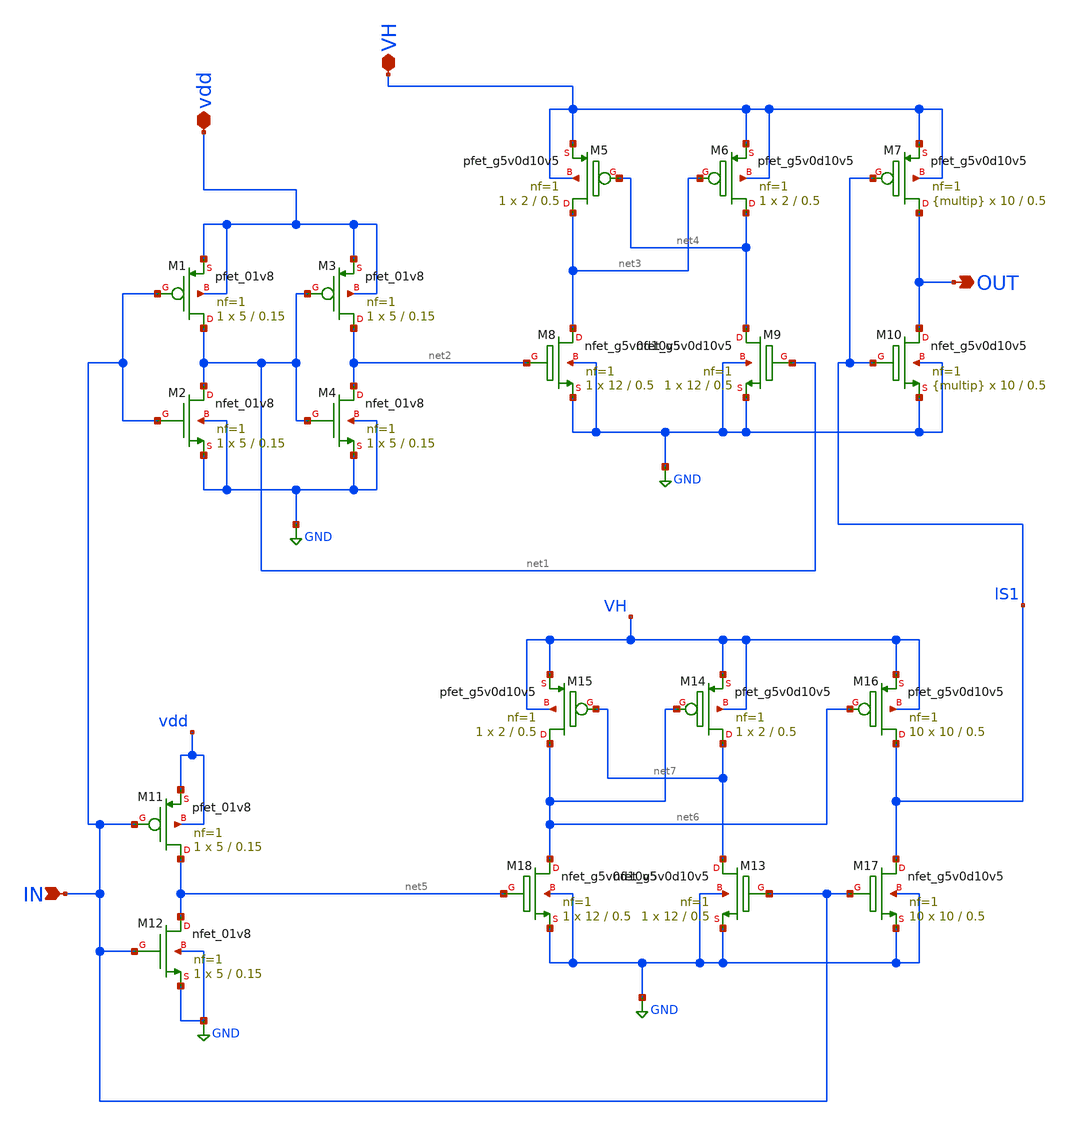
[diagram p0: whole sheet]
** sch_path: xschem/dev_switches/DCDC_10V/LS.sch
**.subckt LS OUT IN VH vdd
*.opin OUT
*.ipin IN
*.iopin VH
*.iopin vdd
XM1 net1 IN vdd vdd sky130_fd_pr__pfet_01v8 L=0.15 W=5 nf=1 ad='int((nf+1)/2) * W/nf * 0.29' as='int((nf+2)/2) * W/nf * 0.29'
+ pd='2*int((nf+1)/2) * (W/nf + 0.29)' ps='2*int((nf+2)/2) * (W/nf + 0.29)' nrd='0.29 / W' nrs='0.29 / W'
+ sa=0 sb=0 sd=0 mult=1 m=1
XM2 net1 IN GND GND sky130_fd_pr__nfet_01v8 L=0.15 W=5 nf=1 ad='int((nf+1)/2) * W/nf * 0.29' as='int((nf+2)/2) * W/nf * 0.29'
+ pd='2*int((nf+1)/2) * (W/nf + 0.29)' ps='2*int((nf+2)/2) * (W/nf + 0.29)' nrd='0.29 / W' nrs='0.29 / W'
+ sa=0 sb=0 sd=0 mult=1 m=1
XM3 net2 net1 vdd vdd sky130_fd_pr__pfet_01v8 L=0.15 W=5 nf=1 ad='int((nf+1)/2) * W/nf * 0.29' as='int((nf+2)/2) * W/nf * 0.29'
+ pd='2*int((nf+1)/2) * (W/nf + 0.29)' ps='2*int((nf+2)/2) * (W/nf + 0.29)' nrd='0.29 / W' nrs='0.29 / W'
+ sa=0 sb=0 sd=0 mult=1 m=1
XM4 net2 net1 GND GND sky130_fd_pr__nfet_01v8 L=0.15 W=5 nf=1 ad='int((nf+1)/2) * W/nf * 0.29' as='int((nf+2)/2) * W/nf * 0.29'
+ pd='2*int((nf+1)/2) * (W/nf + 0.29)' ps='2*int((nf+2)/2) * (W/nf + 0.29)' nrd='0.29 / W' nrs='0.29 / W'
+ sa=0 sb=0 sd=0 mult=1 m=1
XM5 net3 net4 VH VH sky130_fd_pr__pfet_g5v0d10v5 L=0.5 W=2 nf=1 ad='int((nf+1)/2) * W/nf * 0.29' as='int((nf+2)/2) * W/nf * 0.29'
+ pd='2*int((nf+1)/2) * (W/nf + 0.29)' ps='2*int((nf+2)/2) * (W/nf + 0.29)' nrd='0.29 / W' nrs='0.29 / W'
+ sa=0 sb=0 sd=0 mult=1 m=1
XM6 net4 net3 VH VH sky130_fd_pr__pfet_g5v0d10v5 L=0.5 W=2 nf=1 ad='int((nf+1)/2) * W/nf * 0.29' as='int((nf+2)/2) * W/nf * 0.29'
+ pd='2*int((nf+1)/2) * (W/nf + 0.29)' ps='2*int((nf+2)/2) * (W/nf + 0.29)' nrd='0.29 / W' nrs='0.29 / W'
+ sa=0 sb=0 sd=0 mult=1 m=1
XM7 OUT lS1 VH VH sky130_fd_pr__pfet_g5v0d10v5 L=0.5 W=10 nf=1 ad='int((nf+1)/2) * W/nf * 0.29' as='int((nf+2)/2) * W/nf * 0.29'
+ pd='2*int((nf+1)/2) * (W/nf + 0.29)' ps='2*int((nf+2)/2) * (W/nf + 0.29)' nrd='0.29 / W' nrs='0.29 / W'
+ sa=0 sb=0 sd=0 mult={multip} m={multip}
XM8 net3 net2 GND GND sky130_fd_pr__nfet_g5v0d10v5 L=0.5 W=12 nf=1 ad='int((nf+1)/2) * W/nf * 0.29' as='int((nf+2)/2) * W/nf * 0.29'
+ pd='2*int((nf+1)/2) * (W/nf + 0.29)' ps='2*int((nf+2)/2) * (W/nf + 0.29)' nrd='0.29 / W' nrs='0.29 / W'
+ sa=0 sb=0 sd=0 mult=1 m=1
XM9 net4 net1 GND GND sky130_fd_pr__nfet_g5v0d10v5 L=0.5 W=12 nf=1 ad='int((nf+1)/2) * W/nf * 0.29' as='int((nf+2)/2) * W/nf * 0.29'
+ pd='2*int((nf+1)/2) * (W/nf + 0.29)' ps='2*int((nf+2)/2) * (W/nf + 0.29)' nrd='0.29 / W' nrs='0.29 / W'
+ sa=0 sb=0 sd=0 mult=1 m=1
XM10 OUT lS1 GND GND sky130_fd_pr__nfet_g5v0d10v5 L=0.5 W=10 nf=1 ad='int((nf+1)/2) * W/nf * 0.29' as='int((nf+2)/2) * W/nf * 0.29'
+ pd='2*int((nf+1)/2) * (W/nf + 0.29)' ps='2*int((nf+2)/2) * (W/nf + 0.29)' nrd='0.29 / W' nrs='0.29 / W'
+ sa=0 sb=0 sd=0 mult={multip} m={multip}
XM11 net5 IN vdd vdd sky130_fd_pr__pfet_01v8 L=0.15 W=5 nf=1 ad='int((nf+1)/2) * W/nf * 0.29' as='int((nf+2)/2) * W/nf * 0.29'
+ pd='2*int((nf+1)/2) * (W/nf + 0.29)' ps='2*int((nf+2)/2) * (W/nf + 0.29)' nrd='0.29 / W' nrs='0.29 / W'
+ sa=0 sb=0 sd=0 mult=1 m=1
XM12 net5 IN GND GND sky130_fd_pr__nfet_01v8 L=0.15 W=5 nf=1 ad='int((nf+1)/2) * W/nf * 0.29' as='int((nf+2)/2) * W/nf * 0.29'
+ pd='2*int((nf+1)/2) * (W/nf + 0.29)' ps='2*int((nf+2)/2) * (W/nf + 0.29)' nrd='0.29 / W' nrs='0.29 / W'
+ sa=0 sb=0 sd=0 mult=1 m=1
XM15 net6 net7 VH VH sky130_fd_pr__pfet_g5v0d10v5 L=0.5 W=2 nf=1 ad='int((nf+1)/2) * W/nf * 0.29' as='int((nf+2)/2) * W/nf * 0.29'
+ pd='2*int((nf+1)/2) * (W/nf + 0.29)' ps='2*int((nf+2)/2) * (W/nf + 0.29)' nrd='0.29 / W' nrs='0.29 / W'
+ sa=0 sb=0 sd=0 mult=1 m=1
XM14 net7 net6 VH VH sky130_fd_pr__pfet_g5v0d10v5 L=0.5 W=2 nf=1 ad='int((nf+1)/2) * W/nf * 0.29' as='int((nf+2)/2) * W/nf * 0.29'
+ pd='2*int((nf+1)/2) * (W/nf + 0.29)' ps='2*int((nf+2)/2) * (W/nf + 0.29)' nrd='0.29 / W' nrs='0.29 / W'
+ sa=0 sb=0 sd=0 mult=1 m=1
XM16 lS1 net6 VH VH sky130_fd_pr__pfet_g5v0d10v5 L=0.5 W=10 nf=1 ad='int((nf+1)/2) * W/nf * 0.29' as='int((nf+2)/2) * W/nf * 0.29'
+ pd='2*int((nf+1)/2) * (W/nf + 0.29)' ps='2*int((nf+2)/2) * (W/nf + 0.29)' nrd='0.29 / W' nrs='0.29 / W'
+ sa=0 sb=0 sd=0 mult=10 m=10
XM18 net6 net5 GND GND sky130_fd_pr__nfet_g5v0d10v5 L=0.5 W=12 nf=1 ad='int((nf+1)/2) * W/nf * 0.29'
+ as='int((nf+2)/2) * W/nf * 0.29' pd='2*int((nf+1)/2) * (W/nf + 0.29)' ps='2*int((nf+2)/2) * (W/nf + 0.29)'
+ nrd='0.29 / W' nrs='0.29 / W' sa=0 sb=0 sd=0 mult=1 m=1
XM13 net7 IN GND GND sky130_fd_pr__nfet_g5v0d10v5 L=0.5 W=12 nf=1 ad='int((nf+1)/2) * W/nf * 0.29' as='int((nf+2)/2) * W/nf * 0.29'
+ pd='2*int((nf+1)/2) * (W/nf + 0.29)' ps='2*int((nf+2)/2) * (W/nf + 0.29)' nrd='0.29 / W' nrs='0.29 / W'
+ sa=0 sb=0 sd=0 mult=1 m=1
XM17 lS1 IN GND GND sky130_fd_pr__nfet_g5v0d10v5 L=0.5 W=10 nf=1 ad='int((nf+1)/2) * W/nf * 0.29' as='int((nf+2)/2) * W/nf * 0.29'
+ pd='2*int((nf+1)/2) * (W/nf + 0.29)' ps='2*int((nf+2)/2) * (W/nf + 0.29)' nrd='0.29 / W' nrs='0.29 / W'
+ sa=0 sb=0 sd=0 mult=10 m=10
**** begin user architecture code

*
* Parameters

*.PARAM BAT=1.8
.PARAM W12=12 W45=2 LLS=0.5 multip=40
*.option scale=1e-6
*.options TEMP = 65.0

* Models
*.lib /foss/pdk/sky130A/libs.tech/ngspice/sky130.lib.spice TT

*Fuentes******
*VBAT VDD 0 DC BAT
*VHIGH VH 0 DC 5
*vin IN 0 dc 0 PULSE (0 BAT .1n .1n .1n 10n 20n)

*COUT OUT 0 20p


*.options savecurrents
*.save all
*+ @M.XM12.msky130_fd_pr_nfet_01v8[id]

*.control
*tran 0.1n 100n
*plot v(IN) v(LS1) v(OUT) v(net6) i(@M.XM12.msky130_fd_pr_nfet_01v8[id])
*write driver.raw
*.endc
*.end
*

**** end user architecture code
**.ends
.GLOBAL GND
.end
